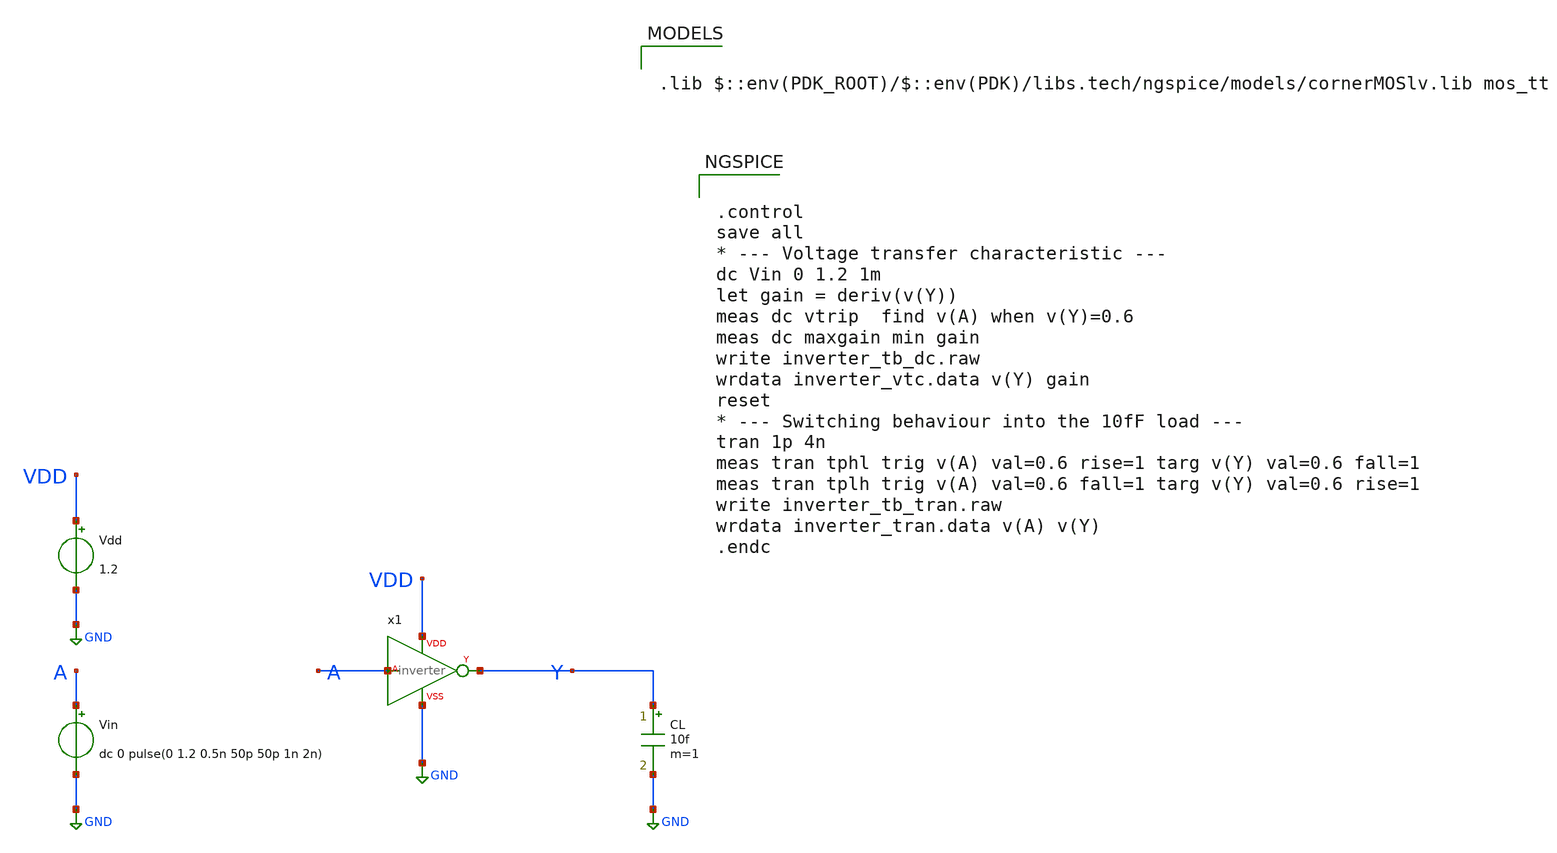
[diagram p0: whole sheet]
** sch_path: analog/xschem/inverter_tb.sch
**.subckt inverter_tb
Vdd VDD GND 1.2
Vin A GND dc 0 pulse(0 1.2 0.5n 50p 50p 1n 2n)
CL Y GND 10f m=1
x1 A Y VDD GND inverter
**** begin user architecture code

.lib $::env(PDK_ROOT)/$::env(PDK)/libs.tech/ngspice/models/cornerMOSlv.lib mos_tt



.control
save all
* --- Voltage transfer characteristic ---
dc Vin 0 1.2 1m
let gain = deriv(v(Y))
meas dc vtrip  find v(A) when v(Y)=0.6
meas dc maxgain min gain
write inverter_tb_dc.raw
wrdata inverter_vtc.data v(Y) gain
reset
* --- Switching behaviour into the 10fF load ---
tran 1p 4n
meas tran tphl trig v(A) val=0.6 rise=1 targ v(Y) val=0.6 fall=1
meas tran tplh trig v(A) val=0.6 fall=1 targ v(Y) val=0.6 rise=1
write inverter_tb_tran.raw
wrdata inverter_tran.data v(A) v(Y)
.endc


**** end user architecture code
**.ends

* expanding   symbol:  /work/analog/xschem/inverter.sym # of pins=4
** sym_path: analog/xschem/inverter.sym
** sch_path: analog/xschem/inverter.sch
.subckt inverter A Y VDD VSS
*.ipin A
*.opin Y
*.iopin VDD
*.iopin VSS
XM1 Y A VDD VDD sg13_lv_pmos w=2.0u l=0.13u ng=1 m=1 mm_ok=1
XM2 Y A VSS VSS sg13_lv_nmos w=1.0u l=0.13u ng=1 m=1 mm_ok=1
.ends

.GLOBAL GND
.end
